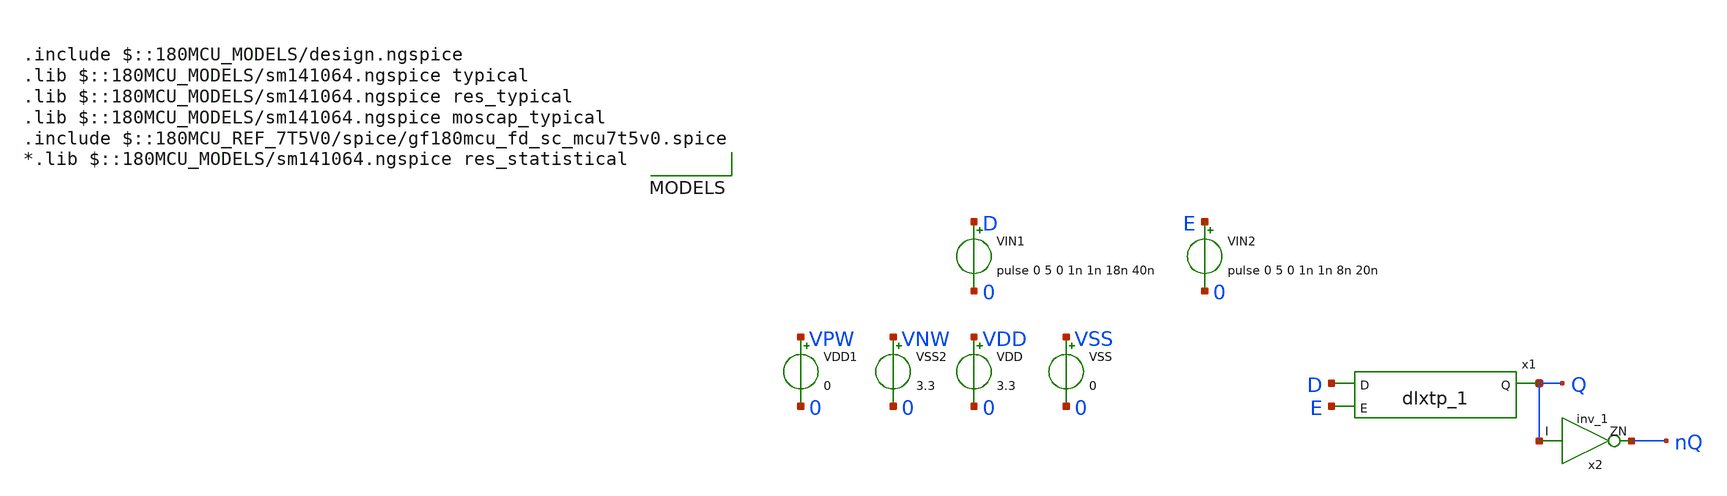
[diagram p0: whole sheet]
** sch_path: DAC/xschem/std_cell/test)latch.sch
**.subckt test)latch
x1 D E Q VDD VNW VPW VSS gf180mcu_fd_sc_mcu7t5v0__latq_1
VDD VDD 0 3.3
VSS VSS 0 0
VDD1 VPW 0 0
VSS2 VNW 0 3.3
VIN1 D 0 pulse 0 5 0 1n 1n 18n 40n
VIN2 E 0 pulse 0 5 0 1n 1n 8n 20n
x2 Q nQ VDD VNW VPW VSS gf180mcu_fd_sc_mcu7t5v0__inv_1
**** begin user architecture code




.control
	tran 0.1n 50n
	plot v(D) V(E)
	plot v(Q) v(nQ)
.endc
.save all





.include $::180MCU_MODELS/design.ngspice
.lib $::180MCU_MODELS/sm141064.ngspice typical
.lib $::180MCU_MODELS/sm141064.ngspice res_typical
.lib $::180MCU_MODELS/sm141064.ngspice moscap_typical
.include $::180MCU_REF_7T5V0/spice/gf180mcu_fd_sc_mcu7t5v0.spice
*.lib $::180MCU_MODELS/sm141064.ngspice res_statistical

**** end user architecture code
**.ends
.end
